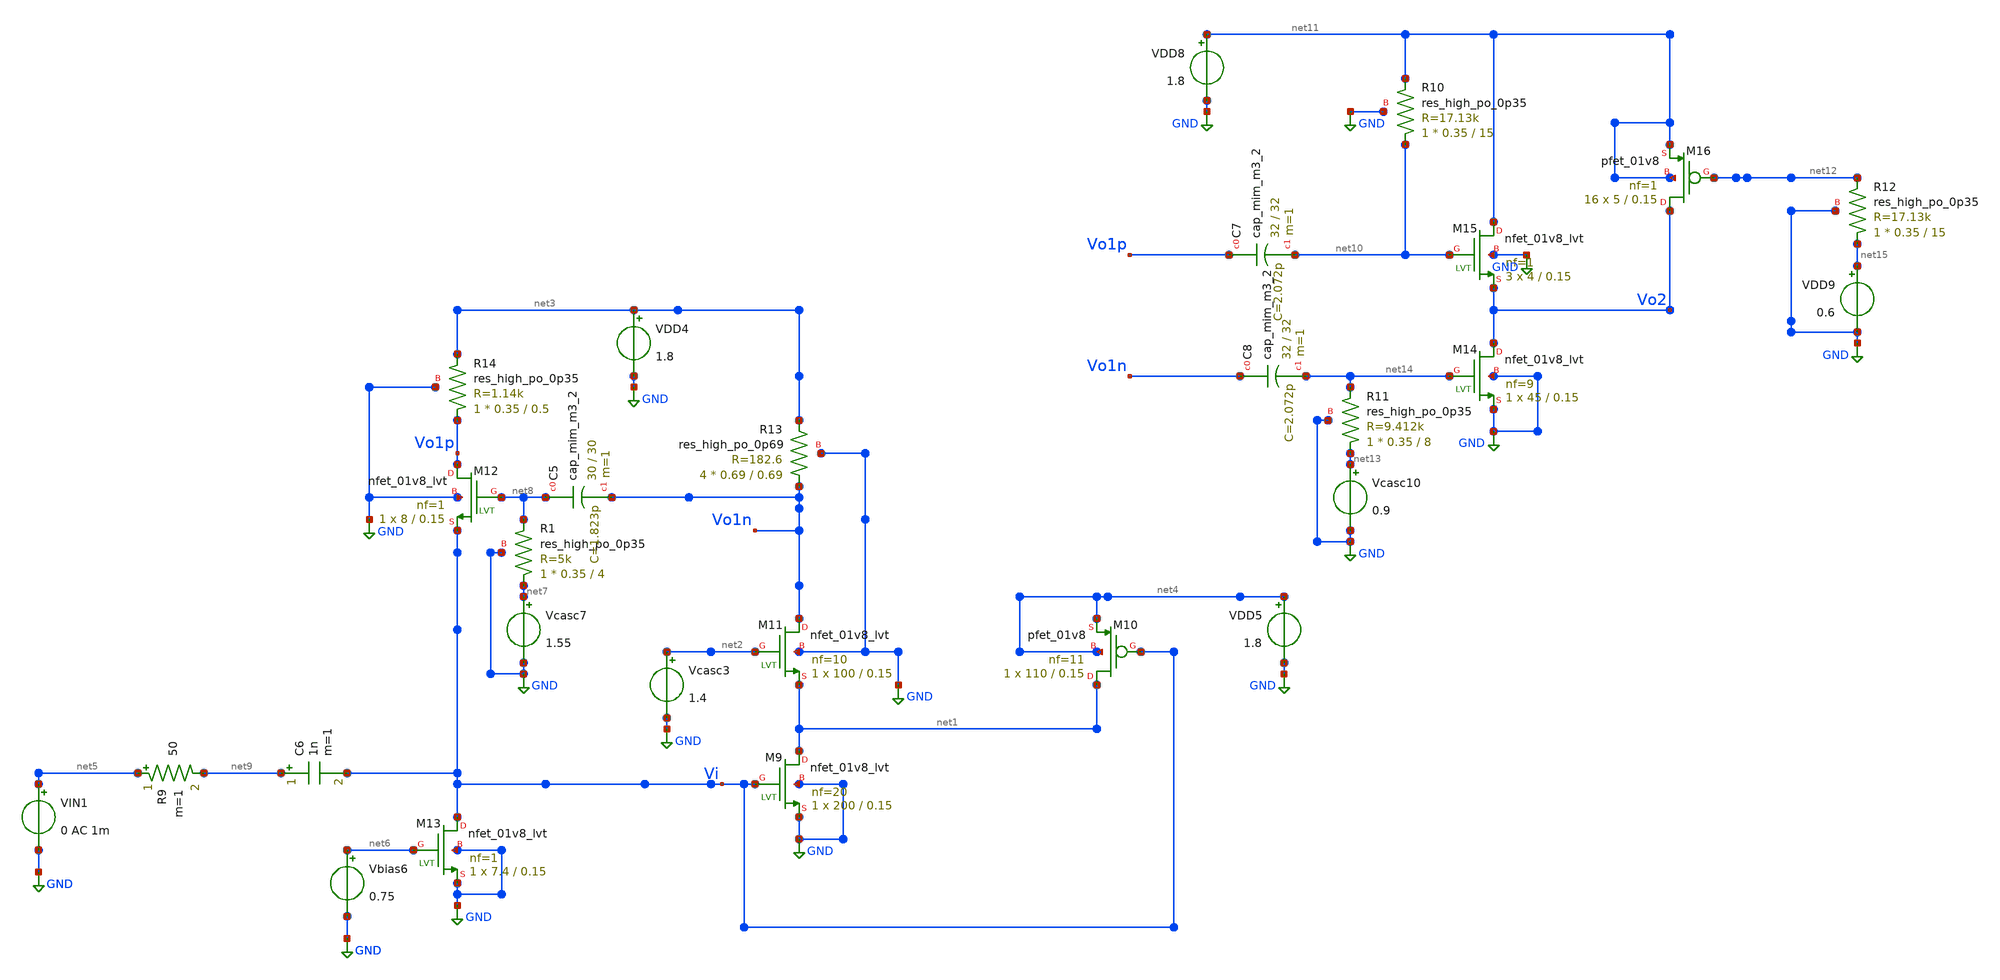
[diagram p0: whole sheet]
** sch_path: xschem/LNA.sch
**.subckt LNA
VIN1 net5 GND 0 AC 1m
Vcasc3 net2 GND 1.4
VDD4 net3 GND 1.8
VDD5 net4 GND 1.8
Vbias6 net6 GND 0.75
Vcasc7 net7 GND 1.55
XR1 net7 net8 GND sky130_fd_pr__res_high_po_0p35 L=4 mult=1 m=1
XC5 net8 Vo1n sky130_fd_pr__cap_mim_m3_2 W=30 L=30 MF=1 m=1
C6 net9 Vi 1n m=1
XM9 net1 Vi GND GND sky130_fd_pr__nfet_01v8_lvt L=0.15 W=200 nf=20 ad='int((nf+1)/2) * W/nf * 0.29' as='int((nf+2)/2) * W/nf * 0.29'
+ pd='2*int((nf+1)/2) * (W/nf + 0.29)' ps='2*int((nf+2)/2) * (W/nf + 0.29)' nrd='0.29 / W' nrs='0.29 / W'
+ sa=0 sb=0 sd=0 mult=1 m=1
XM10 net1 Vi net4 net4 sky130_fd_pr__pfet_01v8 L=0.15 W=110 nf=11 ad='int((nf+1)/2) * W/nf * 0.29' as='int((nf+2)/2) * W/nf * 0.29'
+ pd='2*int((nf+1)/2) * (W/nf + 0.29)' ps='2*int((nf+2)/2) * (W/nf + 0.29)' nrd='0.29 / W' nrs='0.29 / W'
+ sa=0 sb=0 sd=0 mult=1 m=1
XM11 Vo1n net2 net1 GND sky130_fd_pr__nfet_01v8_lvt L=0.15 W=100 nf=10 ad='int((nf+1)/2) * W/nf * 0.29'
+ as='int((nf+2)/2) * W/nf * 0.29' pd='2*int((nf+1)/2) * (W/nf + 0.29)' ps='2*int((nf+2)/2) * (W/nf + 0.29)'
+ nrd='0.29 / W' nrs='0.29 / W' sa=0 sb=0 sd=0 mult=1 m=1
XM12 Vo1p net8 Vi GND sky130_fd_pr__nfet_01v8_lvt L=0.15 W=8 nf=1 ad='int((nf+1)/2) * W/nf * 0.29' as='int((nf+2)/2) * W/nf * 0.29'
+ pd='2*int((nf+1)/2) * (W/nf + 0.29)' ps='2*int((nf+2)/2) * (W/nf + 0.29)' nrd='0.29 / W' nrs='0.29 / W'
+ sa=0 sb=0 sd=0 mult=1 m=1
XM13 Vi net6 GND GND sky130_fd_pr__nfet_01v8_lvt L=0.15 W=7.4 nf=1 ad='int((nf+1)/2) * W/nf * 0.29' as='int((nf+2)/2) * W/nf * 0.29'
+ pd='2*int((nf+1)/2) * (W/nf + 0.29)' ps='2*int((nf+2)/2) * (W/nf + 0.29)' nrd='0.29 / W' nrs='0.29 / W'
+ sa=0 sb=0 sd=0 mult=1 m=1
R9 net5 net9 50 m=1
XM14 Vo2 net14 GND GND sky130_fd_pr__nfet_01v8_lvt L=0.15 W=45 nf=9 ad='int((nf+1)/2) * W/nf * 0.29'
+ as='int((nf+2)/2) * W/nf * 0.29' pd='2*int((nf+1)/2) * (W/nf + 0.29)' ps='2*int((nf+2)/2) * (W/nf + 0.29)'
+ nrd='0.29 / W' nrs='0.29 / W' sa=0 sb=0 sd=0 mult=1 m=1
XM15 net11 net10 Vo2 GND sky130_fd_pr__nfet_01v8_lvt L=0.15 W=4 nf=1 ad='int((nf+1)/2) * W/nf * 0.29'
+ as='int((nf+2)/2) * W/nf * 0.29' pd='2*int((nf+1)/2) * (W/nf + 0.29)' ps='2*int((nf+2)/2) * (W/nf + 0.29)'
+ nrd='0.29 / W' nrs='0.29 / W' sa=0 sb=0 sd=0 mult=3 m=3
XR10 net10 net11 GND sky130_fd_pr__res_high_po_0p35 L=15 mult=1 m=1
XM16 Vo2 net12 net11 net11 sky130_fd_pr__pfet_01v8 L=0.15 W=5 nf=1 ad='int((nf+1)/2) * W/nf * 0.29' as='int((nf+2)/2) * W/nf * 0.29'
+ pd='2*int((nf+1)/2) * (W/nf + 0.29)' ps='2*int((nf+2)/2) * (W/nf + 0.29)' nrd='0.29 / W' nrs='0.29 / W'
+ sa=0 sb=0 sd=0 mult=16 m=16
VDD8 net11 GND 1.8
VDD9 net15 GND 0.6
XC7 Vo1p net10 sky130_fd_pr__cap_mim_m3_2 W=32 L=32 MF=1 m=1
Vcasc10 net13 GND 0.9
XR11 net13 net14 GND sky130_fd_pr__res_high_po_0p35 L=8 mult=1 m=1
XC8 Vo1n net14 sky130_fd_pr__cap_mim_m3_2 W=32 L=32 MF=1 m=1
XR12 net15 net12 GND sky130_fd_pr__res_high_po_0p35 L=15 mult=1 m=1
XR13 Vo1n net3 GND sky130_fd_pr__res_high_po_0p69 L=0.69 mult=4 m=4
XR14 Vo1p net3 GND sky130_fd_pr__res_high_po_0p35 L=0.5 mult=1 m=1
**** begin user architecture code

.lib $::SKYWATER_MODELS/sky130.lib.spice tt




.control
save all
op
	let gm1=@m.xm1.msky130_fd_pr__nfet_01v8_lvt[gm]
	let id1=@m.xm1.msky130_fd_pr__nfet_01v8_lvt[id]
	let gm2=@m.xm2.msky130_fd_pr__pfet_01v8[gm]
	let id2=@m.xm2.msky130_fd_pr__pfet_01v8[id]
	let gm3=@m.xm3.msky130_fd_pr__nfet_01v8_lvt[gm]
	let id3=@m.xm3.msky130_fd_pr__nfet_01v8_lvt[id]
	let gm4=@m.xm4.msky130_fd_pr__nfet_01v8_lvt[gm]
	let id4=@m.xm4.msky130_fd_pr__nfet_01v8_lvt[id]
	let gm5=@m.xm5.msky130_fd_pr__nfet_01v8_lvt[gm]
	let id5=@m.xm5.msky130_fd_pr__nfet_01v8_lvt[id]
	let gm6=@m.xm6.msky130_fd_pr__nfet_01v8_lvt[gm]
	let id6=@m.xm6.msky130_fd_pr__nfet_01v8_lvt[id]
	let gm7=@m.xm7.msky130_fd_pr__nfet_01v8_lvt[gm]
	let id7=@m.xm7.msky130_fd_pr__nfet_01v8_lvt[id]
	let gm8=@m.xm8.msky130_fd_pr__nfet_01v8_lvt[gm]
	let id8=@m.xm8.msky130_fd_pr__nfet_01v8_lvt[id]
	print id1 gm1
	print id2 gm2
	print id3 gm3
	print id4 gm4
	print id5 gm5
	print id6 gm6
	print id7 gm7
	print id8 gm8
	print v(vi)
	print v(vo1n)
	print v(vo1p)

ac dec 40 0.1G 10G

let Zo=50;
let Zin=v(vi)/-i(VIN)
Let S11=mag( (Zin-Zo)/(Zin+Zo) )
plot db(S11)
WRDATA S11.csv db(S11)
plot mag(Zin);



let G1p=db(v(Vo1p)/v(Vi))
let G1n=db(v(Vo1n)/v(Vi))
let G2=db(v(Vo2)/v(Vi))
plot G1p G1n G2
WRDATA Gain.csv G2
set sqrnoise

noise v(Vo1n) VIN dec 40 1G 10G
setplot noise1
let Fn=inoise_spectrum/(8.3e-19)
let NFn=db(Fn) / 2
plot NFn

noise v(Vo1p) VIN dec 40 1G 10G
setplot noise1
let Fp=inoise_spectrum/(8.3e-19)
let NFp=db(Fp) / 2
plot NFp

noise v(Vo1p) VIN dec 40 1G 10G
setplot noise1
let F2=inoise_spectrum/(8.3e-19)
let NF2=db(F2) / 2
plot NF2

WRData Noise.csv NF2

.endc


**** end user architecture code
**.ends
.GLOBAL GND
.end
